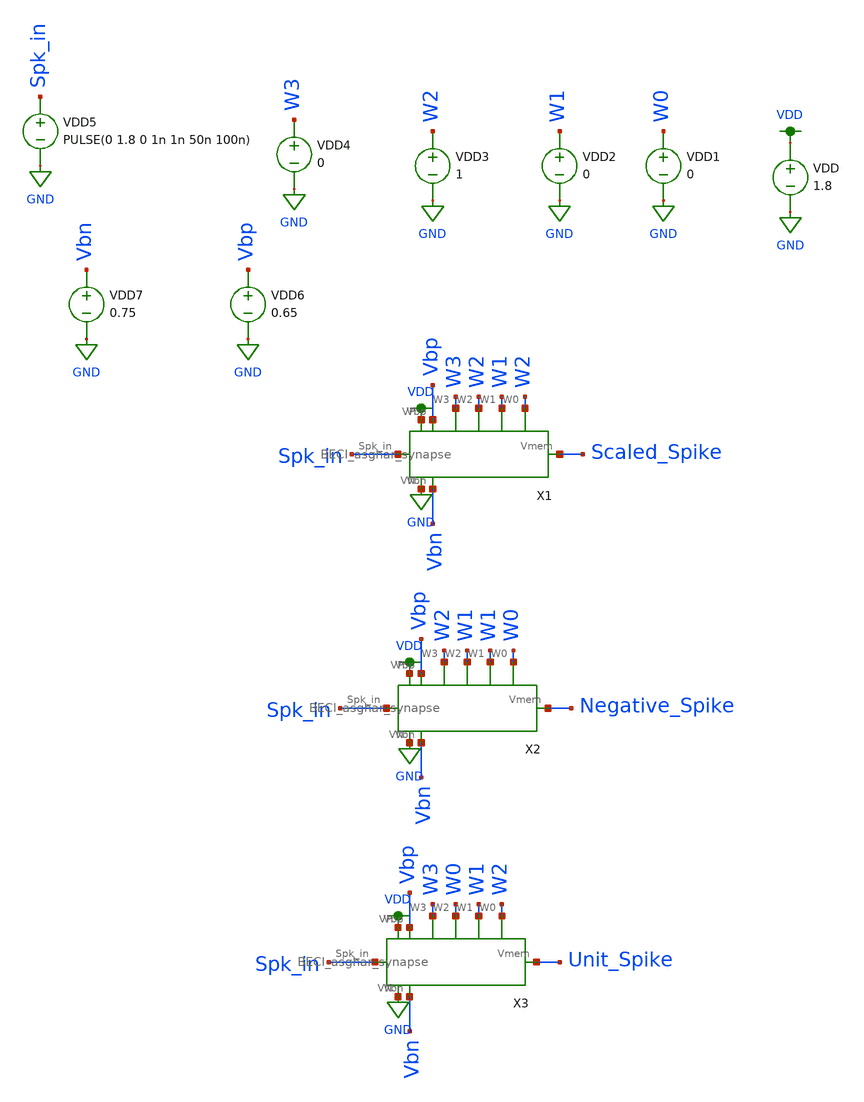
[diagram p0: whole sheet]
** sch_path: schematic/tran_BECI.sch
**.subckt tran_BECI
VDD VDD GND 1.8
VDD1 W0 GND 0
VDD2 W1 GND 0
VDD3 W2 GND 1
VDD4 W3 GND 0
VDD5 Spk_in GND PULSE(0 1.8 0 1n 1n 50n 100n)
VDD6 Vbp GND 0.65
VDD7 Vbn GND 0.75
X1 VDD GND Spk_in Scaled_Spike W3 W2 W1 W2 Vbp Vbn BECI_asghar_synapse
X2 VDD GND Spk_in Negative_Spike W2 W1 W1 W0 Vbp Vbn BECI_asghar_synapse
X3 VDD GND Spk_in Unit_Spike W3 W0 W1 W2 Vbp Vbn BECI_asghar_synapse
**** begin user architecture code

.param W=12
.param L=0.5
.tran 0.01n 1u
.save all


.option wnflag=1
.param MC_SWITCH=0.0
.lib ~/skywater/skywater-pdk/libraries/sky130_fd_pr_ngspice/latest/models/sky130.lib.spice tt

**** end user architecture code
**.ends
.GLOBAL VDD
.GLOBAL GND
.end
